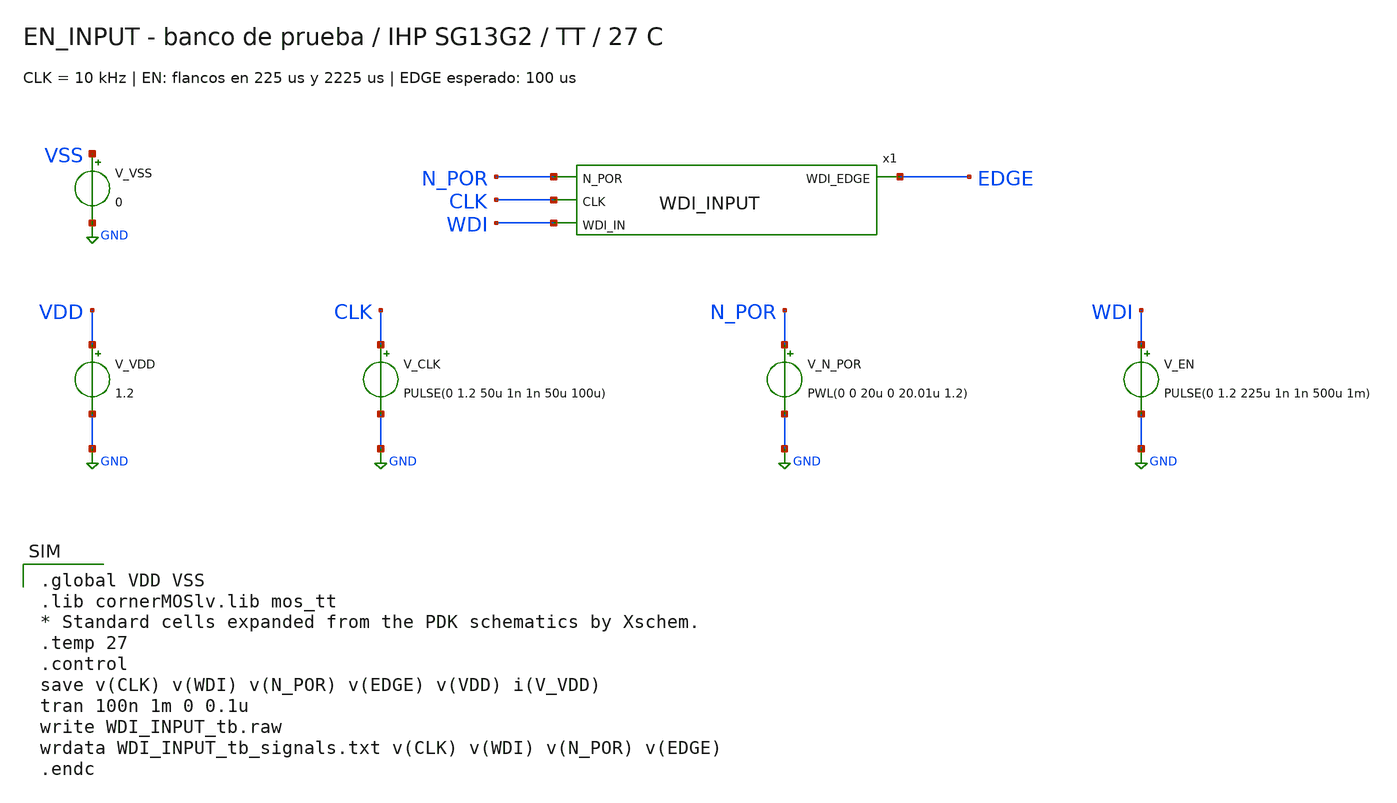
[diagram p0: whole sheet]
** sch_path: design/blocks/wd_input/schematic/WDI_INPUT_tb.sch
**.subckt WDI_INPUT_tb
V_VDD VDD GND 1.2
V_CLK CLK GND PULSE(0 1.2 50u 1n 1n 50u 100u)
V_N_POR N_POR GND PWL(0 0 20u 0 20.01u 1.2)
V_EN WDI GND PULSE(0 1.2 225u 1n 1n 500u 1m)
V_VSS VSS GND 0
x1 N_POR CLK WDI EDGE WDI_INPUT
**** begin user architecture code

.global VDD VSS
.lib cornerMOSlv.lib mos_tt
* Standard cells expanded from the PDK schematics by Xschem.
.temp 27
.control
save v(CLK) v(WDI) v(N_POR) v(EDGE) v(VDD) i(V_VDD)
tran 100n 1m 0 0.1u
write WDI_INPUT_tb.raw
wrdata WDI_INPUT_tb_signals.txt v(CLK) v(WDI) v(N_POR) v(EDGE)
.endc

**** end user architecture code
**.ends
.GLOBAL GND
.end
